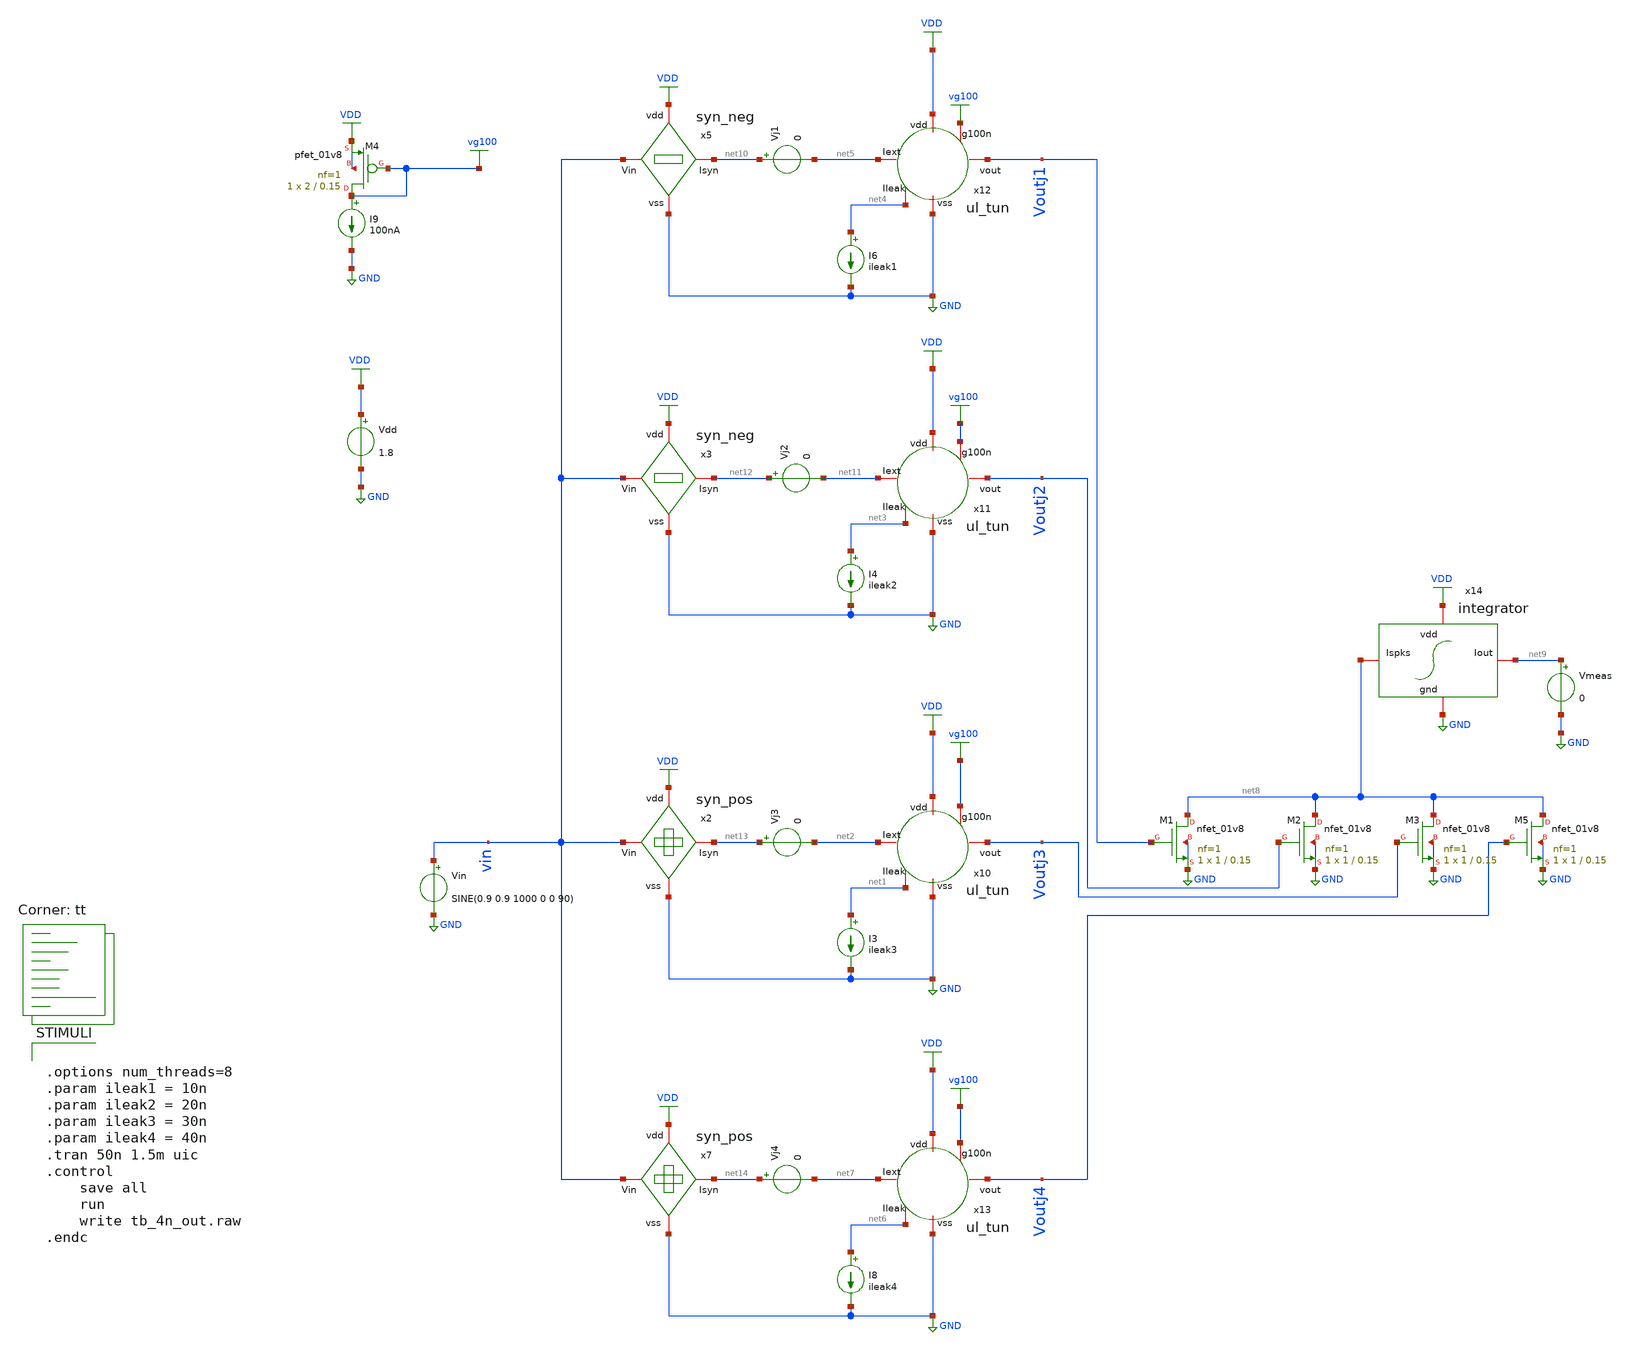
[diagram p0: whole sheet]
** sch_path: tb_4n_out.sch
**.subckt tb_4n_out
Vdd VDD GND 1.8
Vin vin GND SINE(0.9 0.9 1000 0 0 90)
x2 VDD vin net13 GND syn_pos
x3 VDD vin net12 GND syn_neg
x5 VDD vin net10 GND syn_neg
x7 VDD vin net14 GND syn_pos
I9 vg100 GND 100nA
XM4 vg100 vg100 VDD VDD sky130_fd_pr__pfet_01v8 L=0.15 W=2 nf=1 ad='int((nf+1)/2) * W/nf * 0.29' as='int((nf+2)/2) * W/nf * 0.29'
+ pd='2*int((nf+1)/2) * (W/nf + 0.29)' ps='2*int((nf+2)/2) * (W/nf + 0.29)' nrd='0.29 / W' nrs='0.29 / W'
+ sa=0 sb=0 sd=0 mult=1 m=1
I3 net1 GND ileak3
x10 net2 VDD vg100 Voutj3 net1 GND ul_tun
I4 net3 GND ileak2
x11 net11 VDD vg100 Voutj2 net3 GND ul_tun
I6 net4 GND ileak1
x12 net5 VDD vg100 Voutj1 net4 GND ul_tun
I8 net6 GND ileak4
x13 net7 VDD vg100 Voutj4 net6 GND ul_tun
x14 VDD net9 net8 GND integrator
XM1 net8 Voutj1 GND GND sky130_fd_pr__nfet_01v8 L=0.15 W=1 nf=1 ad='int((nf+1)/2) * W/nf * 0.29' as='int((nf+2)/2) * W/nf * 0.29'
+ pd='2*int((nf+1)/2) * (W/nf + 0.29)' ps='2*int((nf+2)/2) * (W/nf + 0.29)' nrd='0.29 / W' nrs='0.29 / W'
+ sa=0 sb=0 sd=0 mult=1 m=1
XM2 net8 Voutj2 GND GND sky130_fd_pr__nfet_01v8 L=0.15 W=1 nf=1 ad='int((nf+1)/2) * W/nf * 0.29' as='int((nf+2)/2) * W/nf * 0.29'
+ pd='2*int((nf+1)/2) * (W/nf + 0.29)' ps='2*int((nf+2)/2) * (W/nf + 0.29)' nrd='0.29 / W' nrs='0.29 / W'
+ sa=0 sb=0 sd=0 mult=1 m=1
XM3 net8 Voutj3 GND GND sky130_fd_pr__nfet_01v8 L=0.15 W=1 nf=1 ad='int((nf+1)/2) * W/nf * 0.29' as='int((nf+2)/2) * W/nf * 0.29'
+ pd='2*int((nf+1)/2) * (W/nf + 0.29)' ps='2*int((nf+2)/2) * (W/nf + 0.29)' nrd='0.29 / W' nrs='0.29 / W'
+ sa=0 sb=0 sd=0 mult=1 m=1
XM5 net8 Voutj4 GND GND sky130_fd_pr__nfet_01v8 L=0.15 W=1 nf=1 ad='int((nf+1)/2) * W/nf * 0.29' as='int((nf+2)/2) * W/nf * 0.29'
+ pd='2*int((nf+1)/2) * (W/nf + 0.29)' ps='2*int((nf+2)/2) * (W/nf + 0.29)' nrd='0.29 / W' nrs='0.29 / W'
+ sa=0 sb=0 sd=0 mult=1 m=1
Vmeas net9 GND 0
Vj1 net10 net5 0
Vj2 net12 net11 0
Vj3 net13 net2 0
Vj4 net14 net7 0
**** begin user architecture code
.lib $::SKYWATER_MODELS/sky130.lib.spice tt
**** end user architecture code
**.ends

* expanding   symbol:  /home/alex/Desktop/EDA/SNN_IPN/Neuron/ultralif/syn_pos.sym # of pins=4
** sym_path: Neuron/ultralif/syn_pos.sym
** sch_path: Neuron/ultralif/syn_pos.sch
.subckt syn_pos vdd Vin Isyn vss
*.iopin Vin
*.iopin vdd
*.iopin vss
*.iopin Isyn
XM9 Isyn vx vdd vdd sky130_fd_pr__pfet_01v8 L=1 W=0.5 nf=1 ad='int((nf+1)/2) * W/nf * 0.29' as='int((nf+2)/2) * W/nf * 0.29'
+ pd='2*int((nf+1)/2) * (W/nf + 0.29)' ps='2*int((nf+2)/2) * (W/nf + 0.29)' nrd='0.29 / W' nrs='0.29 / W'
+ sa=0 sb=0 sd=0 mult=1 m=1
XM10 vx vx vdd vdd sky130_fd_pr__pfet_01v8 L=0.15 W=0.5 nf=1 ad='int((nf+1)/2) * W/nf * 0.29' as='int((nf+2)/2) * W/nf * 0.29'
+ pd='2*int((nf+1)/2) * (W/nf + 0.29)' ps='2*int((nf+2)/2) * (W/nf + 0.29)' nrd='0.29 / W' nrs='0.29 / W'
+ sa=0 sb=0 sd=0 mult=5 m=5
XM12 vx Vin vss vss sky130_fd_pr__nfet_01v8 L=1 W=0.4 nf=1 ad='int((1 + 1)/2) * 0.4 / 1 * 0.29' as='int((1 + 2)/2) * 0.4 / 1 * 0.29'
+ pd='2*int((1 + 1)/2) * (0.4 / 1 + 0.29)' ps='2*int((1 + 2)/2) * (0.4 / 1 + 0.29)' nrd='0.29 / 0.4 ' nrs='0.29 / 0.4 '
+ sa=0 sb=0 sd=0 mult=1 m=1
.ends


* expanding   symbol:  /home/alex/Desktop/EDA/SNN_IPN/Neuron/ultralif/syn_neg.sym # of pins=4
** sym_path: Neuron/ultralif/syn_neg.sym
** sch_path: Neuron/ultralif/syn_neg.sch
.subckt syn_neg vdd Vin Isyn vss
*.iopin Vin
*.iopin Isyn
*.iopin vdd
*.iopin vss
XM10 Isyn Vin vx vdd sky130_fd_pr__pfet_01v8 L=35 W=0.5 nf=1 ad='int((nf+1)/2) * W/nf * 0.29' as='int((nf+2)/2) * W/nf * 0.29'
+ pd='2*int((nf+1)/2) * (W/nf + 0.29)' ps='2*int((nf+2)/2) * (W/nf + 0.29)' nrd='0.29 / W' nrs='0.29 / W'
+ sa=0 sb=0 sd=0 mult=1 m=1
XM1 vx Vin vdd vdd sky130_fd_pr__pfet_01v8 L=35 W=0.5 nf=1 ad='int((nf+1)/2) * W/nf * 0.29' as='int((nf+2)/2) * W/nf * 0.29'
+ pd='2*int((nf+1)/2) * (W/nf + 0.29)' ps='2*int((nf+2)/2) * (W/nf + 0.29)' nrd='0.29 / W' nrs='0.29 / W'
+ sa=0 sb=0 sd=0 mult=1 m=1
XM2 Isyn net1 vdd vdd sky130_fd_pr__pfet_01v8 L=1 W=0.5 nf=1 ad='int((nf+1)/2) * W/nf * 0.29' as='int((nf+2)/2) * W/nf * 0.29'
+ pd='2*int((nf+1)/2) * (W/nf + 0.29)' ps='2*int((nf+2)/2) * (W/nf + 0.29)' nrd='0.29 / W' nrs='0.29 / W'
+ sa=0 sb=0 sd=0 mult=1 m=1
XR1 net1 vdd sky130_fd_pr__res_generic_po W=1.15 L=1 m=1
XR2 vss net1 sky130_fd_pr__res_generic_po W=1 L=1 m=1
.ends


* expanding   symbol:  /home/alex/Desktop/EDA/SNN_IPN/Neuron/ultralif/ul_tun.sym # of pins=6
** sym_path: Neuron/ultralif/ul_tun.sym
** sch_path: Neuron/ultralif/ul_tun.sch
.subckt ul_tun Iext vdd g100n vout Ileak vss
*.iopin Iext
*.iopin vout
*.iopin vss
*.iopin Ileak
*.iopin vdd
*.iopin g100n
XM1 Ileak Ileak net1 vdd sky130_fd_pr__pfet_01v8 L=10 W=1 nf=1 ad='int((nf+1)/2) * W/nf * 0.29' as='int((nf+2)/2) * W/nf * 0.29'
+ pd='2*int((nf+1)/2) * (W/nf + 0.29)' ps='2*int((nf+2)/2) * (W/nf + 0.29)' nrd='0.29 / W' nrs='0.29 / W'
+ sa=0 sb=0 sd=0 mult=1 m=1
XM2 Ileak net2 net1 vdd sky130_fd_pr__pfet_01v8 L=0.15 W=1.5 nf=1 ad='int((nf+1)/2) * W/nf * 0.29' as='int((nf+2)/2) * W/nf * 0.29'
+ pd='2*int((nf+1)/2) * (W/nf + 0.29)' ps='2*int((nf+2)/2) * (W/nf + 0.29)' nrd='0.29 / W' nrs='0.29 / W'
+ sa=0 sb=0 sd=0 mult=1 m=1
XM3 net2 net2 net1 vdd sky130_fd_pr__pfet_01v8 L=0.15 W=15 nf=1 ad='int((nf+1)/2) * W/nf * 0.29' as='int((nf+2)/2) * W/nf * 0.29'
+ pd='2*int((nf+1)/2) * (W/nf + 0.29)' ps='2*int((nf+2)/2) * (W/nf + 0.29)' nrd='0.29 / W' nrs='0.29 / W'
+ sa=0 sb=0 sd=0 mult=1 m=1
XM4 net2 Ileak vss vss sky130_fd_pr__nfet_01v8 L=4 W=1 nf=1 ad='int((1 + 1)/2) * 1 / 1 * 0.29' as='int((1 + 2)/2) * 1 / 1 * 0.29'
+ pd='2*int((1 + 1)/2) * (1 / 1 + 0.29)' ps='2*int((1 + 2)/2) * (1 / 1 + 0.29)' nrd='0.29 / 1 ' nrs='0.29 / 1 '
+ sa=0 sb=0 sd=0 mult=1 m=1
C1 net1 vss 1p m=1
XM5 vout_n Ileak vss vss sky130_fd_pr__nfet_01v8 L=0.15 W=1 nf=1 ad='int((1 + 1)/2) * 1 / 1 * 0.29' as='int((1 + 2)/2) * 1 / 1 * 0.29'
+ pd='2*int((1 + 1)/2) * (1 / 1 + 0.29)' ps='2*int((1 + 2)/2) * (1 / 1 + 0.29)' nrd='0.29 / 1 ' nrs='0.29 / 1 '
+ sa=0 sb=0 sd=0 mult=1 m=1
XM6 vout_n g100n vdd vdd sky130_fd_pr__pfet_01v8 L=0.15 W=2 nf=1 ad='int((nf+1)/2) * W/nf * 0.29' as='int((nf+2)/2) * W/nf * 0.29'
+ pd='2*int((nf+1)/2) * (W/nf + 0.29)' ps='2*int((nf+2)/2) * (W/nf + 0.29)' nrd='0.29 / W' nrs='0.29 / W'
+ sa=0 sb=0 sd=0 mult=1 m=1
XM7 vout vout_n vss vss sky130_fd_pr__nfet_01v8 L=0.15 W=1 nf=1 ad='int((1 + 1)/2) * 1 / 1 * 0.29' as='int((1 + 2)/2) * 1 / 1 * 0.29'
+ pd='2*int((1 + 1)/2) * (1 / 1 + 0.29)' ps='2*int((1 + 2)/2) * (1 / 1 + 0.29)' nrd='0.29 / 1 ' nrs='0.29 / 1 '
+ sa=0 sb=0 sd=0 mult=1 m=1
XM8 vout vout_n vdd vdd sky130_fd_pr__pfet_01v8 L=0.15 W=2 nf=1 ad='int((nf+1)/2) * W/nf * 0.29' as='int((nf+2)/2) * W/nf * 0.29'
+ pd='2*int((nf+1)/2) * (W/nf + 0.29)' ps='2*int((nf+2)/2) * (W/nf + 0.29)' nrd='0.29 / W' nrs='0.29 / W'
+ sa=0 sb=0 sd=0 mult=1 m=1
vext Iext net1 0
**** begin user architecture code


.save i(vext)


**** end user architecture code
.ends


* expanding   symbol:  /home/alex/Desktop/EDA/SNN_IPN/Neuron/ultralif/integrator.sym # of pins=4
** sym_path: Neuron/ultralif/integrator.sym
** sch_path: Neuron/ultralif/integrator.sch
.subckt integrator vdd Iout Ispks gnd
*.iopin Ispks
*.iopin Iout
*.iopin vdd
*.iopin gnd
XMIn Ispks vx vsyn vdd sky130_fd_pr__pfet_01v8 L=0.15 W=5 nf=1 ad='int((nf+1)/2) * W/nf * 0.29' as='int((nf+2)/2) * W/nf * 0.29'
+ pd='2*int((nf+1)/2) * (W/nf + 0.29)' ps='2*int((nf+2)/2) * (W/nf + 0.29)' nrd='0.29 / W' nrs='0.29 / W'
+ sa=0 sb=0 sd=0 mult=1 m=1
XM3 vsyn vdd vdd vdd sky130_fd_pr__pfet_01v8 L=0.15 W=5 nf=1 ad='int((nf+1)/2) * W/nf * 0.29' as='int((nf+2)/2) * W/nf * 0.29'
+ pd='2*int((nf+1)/2) * (W/nf + 0.29)' ps='2*int((nf+2)/2) * (W/nf + 0.29)' nrd='0.29 / W' nrs='0.29 / W'
+ sa=0 sb=0 sd=0 mult=1 m=1
XM4 Iout vsyn vdd vdd sky130_fd_pr__pfet_01v8 L=0.15 W=24.5 nf=1 ad='int((nf+1)/2) * W/nf * 0.29' as='int((nf+2)/2) * W/nf * 0.29'
+ pd='2*int((nf+1)/2) * (W/nf + 0.29)' ps='2*int((nf+2)/2) * (W/nf + 0.29)' nrd='0.29 / W' nrs='0.29 / W'
+ sa=0 sb=0 sd=0 mult=1 m=1
XCsyn vdd vsyn sky130_fd_pr__cap_mim_m3_1 W=22.5 L=22 MF=1 m=1
XR2 vx vdd sky130_fd_pr__res_generic_po W=1 L=1 m=1
XR1 gnd vx sky130_fd_pr__res_generic_po W=1 L=1 m=1
.ends

.GLOBAL GND
.GLOBAL VDD
.GLOBAL vg100
**** begin user architecture code


.options num_threads=8
.param ileak1 = 10n
.param ileak2 = 20n
.param ileak3 = 30n
.param ileak4 = 40n
.tran 50n 1.5m uic
.control
	save all
	run
	write tb_4n_out.raw
.endc


**** end user architecture code
.end
